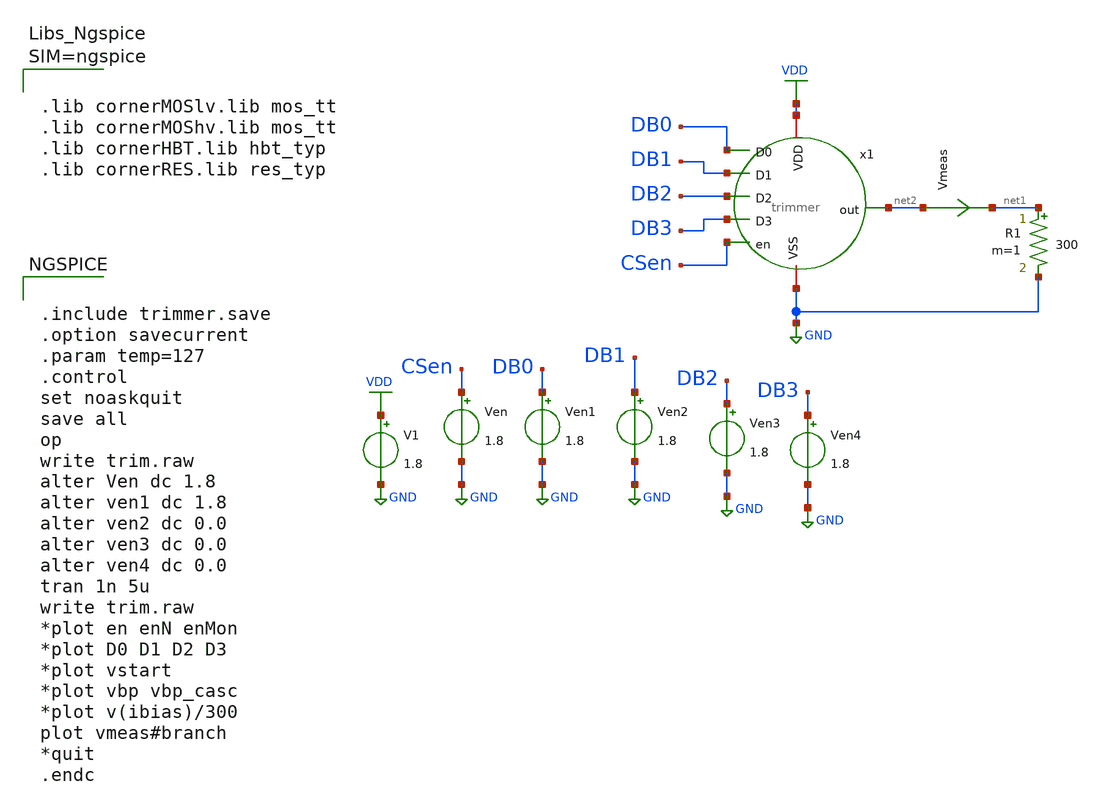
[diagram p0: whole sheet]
** sch_path: blocks/composite/dpi_adexp_neuron/design_data/xschem/trimmer_test.sch
**.subckt trimmer_test
V1 VDD GND 1.8
Ven CSen GND 1.8
Ven1 DB0 GND 1.8
Ven2 DB1 GND 1.8
Ven3 DB2 GND 1.8
Ven4 DB3 GND 1.8
x1 DB0 DB1 DB2 DB3 VDD GND CSen net2 trimmer
R1 net1 GND 300 m=1
Vmeas net2 net1 0
.save i(vmeas)
**** begin user architecture code


.include trimmer.save
.option savecurrent
.param temp=127
.control
set noaskquit
save all
op
write trim.raw
alter Ven dc 1.8
alter ven1 dc 1.8
alter ven2 dc 0.0
alter ven3 dc 0.0
alter ven4 dc 0.0
tran 1n 5u
write trim.raw
*plot en enN enMon
*plot D0 D1 D2 D3
*plot vstart
*plot vbp vbp_casc
*plot v(ibias)/300
plot vmeas#branch
*quit
.endc





.lib cornerMOSlv.lib mos_tt
.lib cornerMOShv.lib mos_tt
.lib cornerHBT.lib hbt_typ
.lib cornerRES.lib res_typ



**** end user architecture code
**.ends

* expanding   symbol:  trimmer.sym # of pins=8
** sym_path: blocks/composite/dpi_adexp_neuron/design_data/xschem/trimmer.sym
** sch_path: blocks/composite/dpi_adexp_neuron/design_data/xschem/trimmer.sch
.subckt trimmer D0 D1 D2 D3 VDD VSS en out
*.ipin en
*.ipin D0
*.ipin D1
*.ipin D2
*.ipin D3
*.opin out
*.iopin VDD
*.iopin VSS
XMP1 net1 net1 net12 VDD sg13_lv_pmos w=0.28u l=8.0u ng=1 m=1 mm_ok=1
XMP2 vstart vstart net1 VDD sg13_lv_pmos w=0.28u l=8.0u ng=1 m=1 mm_ok=1
XMN2 net3 vstart GND GND sg13_lv_nmos w=0.28u l=8.0u ng=1 m=1 mm_ok=1
XMN1 vstart vstart GND GND sg13_lv_nmos w=0.28u l=8.0u ng=1 m=1 mm_ok=1
XMP3 net2 vbp net11 VDD sg13_lv_pmos w=2.0u l=2.0u ng=2 m=1 mm_ok=1
XMP4 net3 vbp_casc net2 VDD sg13_lv_pmos w=2.0u l=0.28u ng=1 m=2 mm_ok=1
XMP5 net4 vbp net10 VDD sg13_lv_pmos w=2.0u l=2.0u ng=1 m=2 mm_ok=1
XMP6 net6 vbp_casc net4 VDD sg13_lv_pmos w=2.0u l=0.28u ng=1 m=2 mm_ok=1
XMP7 net5 vbp net9 VDD sg13_lv_pmos w=2.0u l=2.0u ng=1 m=2 mm_ok=1
XMP8 vbp vbp_casc net5 VDD sg13_lv_pmos w=2.0u l=0.28u ng=1 m=2 mm_ok=1
XMP9 net6 net3 VDD VDD sg13_lv_pmos w=0.28u l=8.0u ng=1 m=1 mm_ok=1
XMN3 net6 net6 GND GND sg13_lv_nmos w=2.0u l=2.0u ng=1 m=1 mm_ok=1
XMN4 vbp_casc net6 net7 GND sg13_lv_nmos w=2.0u l=2.0u ng=1 m=4 mm_ok=1
XR1 vbp vbp_casc sub! rppd w=0.5e-6 l=389e-6 m=1 b=0 mm_ok=1
XR2 net7 GND sub! rhigh w=0.5e-6 l=152.5e-6 m=1 b=0 mm_ok=1
XMP10 net13 vbp net14 VDD sg13_lv_pmos w=2.0u l=2.0u ng=1 m=2 mm_ok=1
XMP11 out vbp_casc net13 VDD sg13_lv_pmos w=2.0u l=0.28u ng=1 m=2 mm_ok=1
XMP16 vbp_casc enMon VDD VDD sg13_lv_pmos w=2.0u l=0.28u ng=1 m=1 mm_ok=1
XMP17 net9 net8 VDD VDD sg13_lv_pmos w=2.0u l=0.28u ng=1 m=2 mm_ok=1
XMP18 net10 net8 VDD VDD sg13_lv_pmos w=2.0u l=0.28u ng=1 m=2 mm_ok=1
XMP19 net12 net8 VDD VDD sg13_lv_pmos w=2.0u l=0.28u ng=1 m=1 mm_ok=1
XMP20 net11 net8 VDD VDD sg13_lv_pmos w=2.0u l=0.28u ng=1 m=1 mm_ok=1
XMN5 vstart net8 GND GND sg13_lv_nmos w=2u l=0.28u ng=1 m=1 mm_ok=1
XMN6 net6 net8 GND GND sg13_lv_nmos w=2u l=0.28u ng=1 m=1 mm_ok=1
xinv2 VDD net8 enMon GND inv
XMP12 net14 net15 VDD VDD sg13_lv_pmos w=2.0u l=0.28u ng=1 m=2 mm_ok=1
XMP13 net16 vbp net17 VDD sg13_lv_pmos w=2.0u l=2.0u ng=1 m=4 mm_ok=1
XMP14 out vbp_casc net16 VDD sg13_lv_pmos w=2.0u l=0.28u ng=1 m=4 mm_ok=1
XMP15 net17 net18 VDD VDD sg13_lv_pmos w=2.0u l=0.28u ng=1 m=2 mm_ok=1
XMP21 net19 vbp net20 VDD sg13_lv_pmos w=2.0u l=2.0u ng=1 m=8 mm_ok=1
XMP22 out vbp_casc net19 VDD sg13_lv_pmos w=2.0u l=0.28u ng=1 m=8 mm_ok=1
XMP23 net20 net21 VDD VDD sg13_lv_pmos w=2.0u l=0.28u ng=1 m=2 mm_ok=1
XMP24 net22 vbp net23 VDD sg13_lv_pmos w=2.0u l=2.0u ng=1 m=16 mm_ok=1
XMP25 out vbp_casc net22 VDD sg13_lv_pmos w=2.0u l=0.28u ng=1 m=16 mm_ok=1
XMP26 net23 net24 VDD VDD sg13_lv_pmos w=2.0u l=0.28u ng=1 m=2 mm_ok=1
xinv6 VDD en net8 GND inv
xinv3 VDD D0 net15 GND inv
xinv7 VDD D1 net18 GND inv
xinv8 VDD D2 net21 GND inv
xinv9 VDD D3 net24 GND inv
.ends


* expanding   symbol:  inv.sym # of pins=4
** sym_path: blocks/composite/dpi_adexp_neuron/design_data/xschem/dev/inv.sym
** sch_path: blocks/composite/dpi_adexp_neuron/design_data/xschem/dev/inv.sch
.subckt inv VDD in out VSS
*.iopin VDD
*.ipin in
*.iopin VSS
*.opin out
XM1 out in VSS VSS sg13_lv_nmos w=2.0u l=0.28u ng=1 m=1 mm_ok=1
XM2 out in VDD VDD sg13_lv_pmos w=2.0u l=0.28u ng=1 m=1 mm_ok=1
.ends

.GLOBAL GND
.GLOBAL VDD
.end
